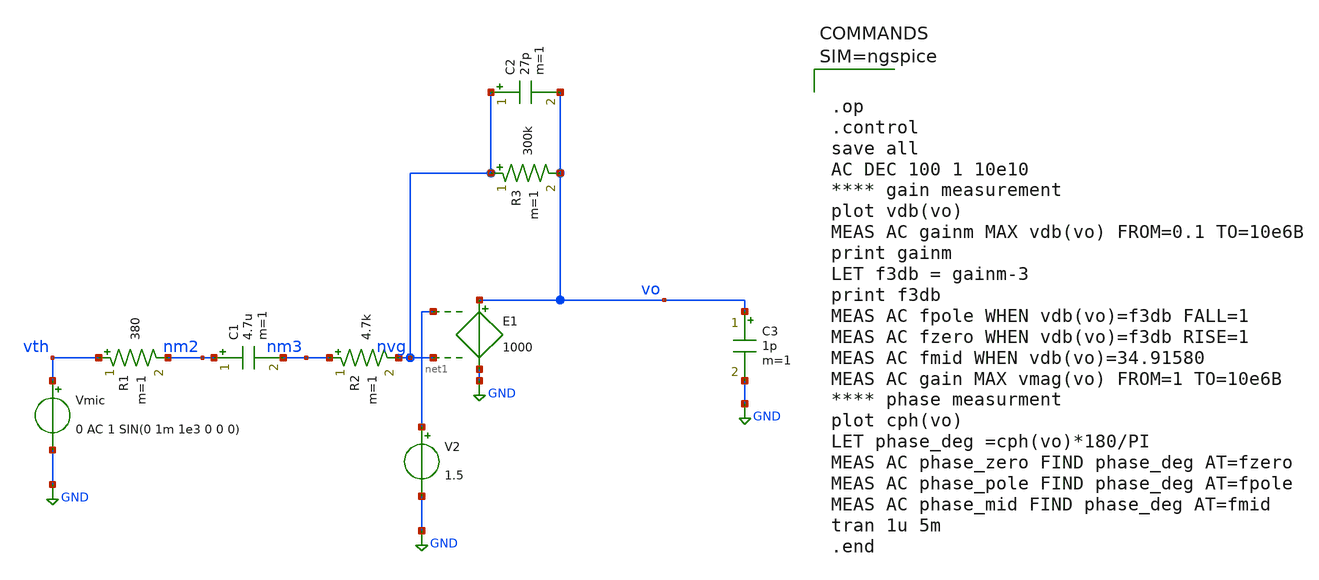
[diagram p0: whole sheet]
** sch_path: Work/xschem/untitled.sch
**.subckt untitled
Vmic vth GND 0 AC 1 SIN(0 1m 1e3 0 0 0)
R1 vth nm2 380 m=1
C1 nm2 nm3 4.7u m=1
R2 nm3 nvg 4.7k m=1
E1 vo GND net1 nvg 1000
R3 nvg vo 300k m=1
C2 nvg vo 27p m=1
V2 net1 GND 1.5
C3 vo GND 1p m=1
**** begin user architecture code



.op
.control
save all
AC DEC 100 1 10e10
**** gain measurement
plot vdb(vo)
MEAS AC gainm MAX vdb(vo) FROM=0.1 TO=10e6B
print gainm
LET f3db = gainm-3
print f3db
MEAS AC fpole WHEN vdb(vo)=f3db FALL=1
MEAS AC fzero WHEN vdb(vo)=f3db RISE=1
MEAS AC fmid WHEN vdb(vo)=34.91580
MEAS AC gain MAX vmag(vo) FROM=1 TO=10e6B
**** phase measurment
plot cph(vo)
LET phase_deg =cph(vo)*180/PI
MEAS AC phase_zero FIND phase_deg AT=fzero
MEAS AC phase_pole FIND phase_deg AT=fpole
MEAS AC phase_mid FIND phase_deg AT=fmid
tran 1u 5m
.end



**** end user architecture code
**.ends
.GLOBAL GND
.end
